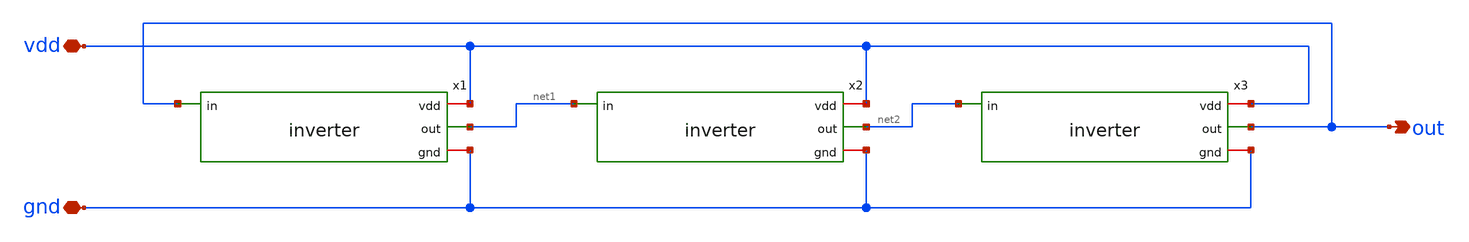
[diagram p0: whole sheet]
** sch_path: ring_osc.sch
**.subckt ring_osc vdd gnd out
*.iopin vdd
*.iopin gnd
*.opin out
x1 vdd out net1 gnd inverter
x2 vdd net1 net2 gnd inverter
x3 vdd net2 out gnd inverter
**.ends

* expanding   symbol:  /home/mona121130125/percobaan_layout/inverter.sym # of pins=4
** sym_path: inverter.sym
** sch_path: inverter.sch
.subckt inverter vdd in out gnd
*.ipin in
*.opin out
*.iopin vdd
*.iopin gnd
XM1 out in vdd vdd sky130_fd_pr__pfet_01v8 L=0.15 W=1 nf=1 ad='int((nf+1)/2) * W/nf * 0.29' as='int((nf+2)/2) * W/nf * 0.29'
+ pd='2*int((nf+1)/2) * (W/nf + 0.29)' ps='2*int((nf+2)/2) * (W/nf + 0.29)' nrd='0.29 / W' nrs='0.29 / W'
+ sa=0 sb=0 sd=0 mult=1 m=1
XM2 out in gnd gnd sky130_fd_pr__nfet_01v8 L=0.15 W=1 nf=1 ad='int((nf+1)/2) * W/nf * 0.29' as='int((nf+2)/2) * W/nf * 0.29'
+ pd='2*int((nf+1)/2) * (W/nf + 0.29)' ps='2*int((nf+2)/2) * (W/nf + 0.29)' nrd='0.29 / W' nrs='0.29 / W'
+ sa=0 sb=0 sd=0 mult=1 m=1
.ends

.end
